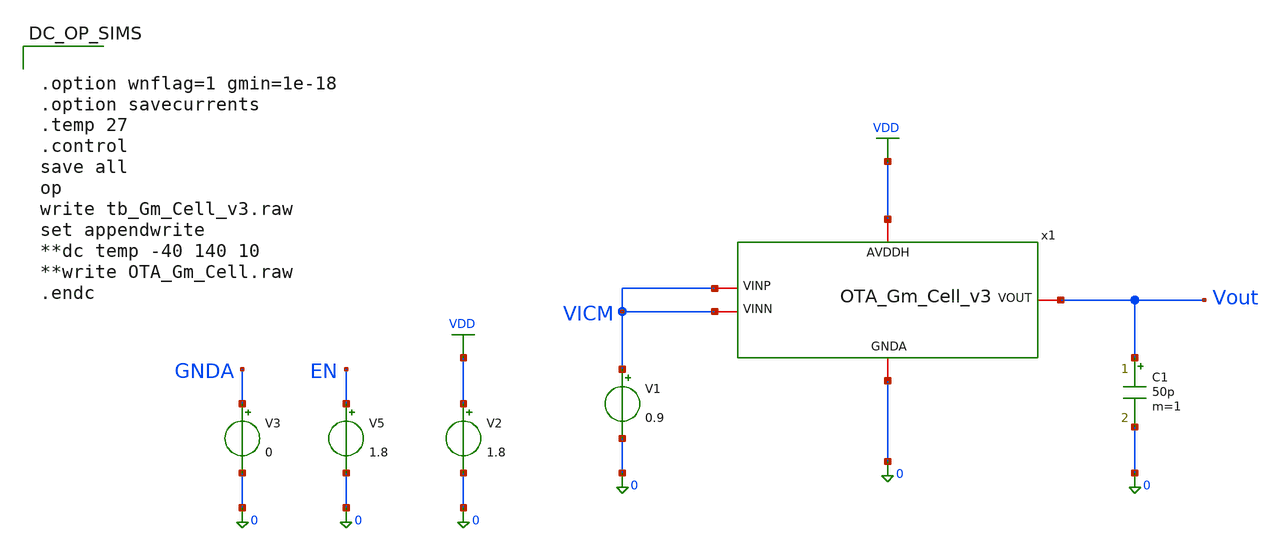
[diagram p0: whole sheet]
** sch_path: OTAs/NMOS_SrcDeg_SE_OTA_IntBias/SCH/tb_Gm_Cell_v3.sch
.lib $::SKYWATER_MODELS/sky130.lib.spice tt_mm
.include $::SKYWATER_STDCELLS/sky130_fd_sc_hd.spice

**.subckt tb_Gm_Cell_v3
x1 VDD VICM VICM Vout 0 OTA_Gm_Cell_v3
V1 VICM 0 0.9
V2 VDD 0 1.8
V3 GNDA 0 0
V5 EN 0 1.8
C1 Vout 0 50p m=1
**** begin user architecture code



.save @m.x1.xm1.msky130_fd_pr__nfet_01v8[gm]
.save @m.x1.xm1.msky130_fd_pr__nfet_01v8[gds]
.save @m.x1.xm1.msky130_fd_pr__nfet_01v8[vth]
.save @m.x1.xm1.msky130_fd_pr__nfet_01v8[vdsat]
.save @m.x1.xm1.msky130_fd_pr__nfet_01v8[cgg]
.save @m.x1.xm1.msky130_fd_pr__nfet_01v8[cgso]
.save @m.x1.xm1.msky130_fd_pr__nfet_01v8[cgdo]
.save @m.x1.xm3.msky130_fd_pr__pfet_01v8[gm]
.save @m.x1.xm3.msky130_fd_pr__pfet_01v8[gds]
.save @m.x1.xm3.msky130_fd_pr__pfet_01v8[vth]
.save @m.x1.xm3.msky130_fd_pr__pfet_01v8[vdsat]
.save @m.x1.xm3.msky130_fd_pr__pfet_01v8[cgg]
.save @m.x1.xm3.msky130_fd_pr__pfet_01v8[cgso]
.save @m.x1.xm3.msky130_fd_pr__pfet_01v8[cgdo]
.save @m.x1.xm4.msky130_fd_pr__pfet_01v8[gm]
.save @m.x1.xm4.msky130_fd_pr__pfet_01v8[gds]
.save @m.x1.xm4.msky130_fd_pr__pfet_01v8[vth]
.save @m.x1.xm4.msky130_fd_pr__pfet_01v8[vdsat]
.save @m.x1.xm4.msky130_fd_pr__pfet_01v8[cgg]
.save @m.x1.xm4.msky130_fd_pr__pfet_01v8[cgso]
.save @m.x1.xm4.msky130_fd_pr__pfet_01v8[cgdo]
.save @m.x1.xm5.msky130_fd_pr__pfet_01v8[gm]
.save @m.x1.xm5.msky130_fd_pr__pfet_01v8[gds]
.save @m.x1.xm5.msky130_fd_pr__pfet_01v8[vth]
.save @m.x1.xm5.msky130_fd_pr__pfet_01v8[vdsat]
.save @m.x1.xm5.msky130_fd_pr__pfet_01v8[cgg]
.save @m.x1.xm5.msky130_fd_pr__pfet_01v8[cgso]
.save @m.x1.xm5.msky130_fd_pr__pfet_01v8[cgdo]
.save @m.x1.xm6.msky130_fd_pr__pfet_01v8[gm]
.save @m.x1.xm6.msky130_fd_pr__pfet_01v8[gds]
.save @m.x1.xm6.msky130_fd_pr__pfet_01v8[vth]
.save @m.x1.xm6.msky130_fd_pr__pfet_01v8[vdsat]
.save @m.x1.xm6.msky130_fd_pr__pfet_01v8[cgg]
.save @m.x1.xm6.msky130_fd_pr__pfet_01v8[cgso]
.save @m.x1.xm6.msky130_fd_pr__pfet_01v8[cgdo]
.save @m.x1.xm7.msky130_fd_pr__nfet_01v8[gm]
.save @m.x1.xm7.msky130_fd_pr__nfet_01v8[gds]
.save @m.x1.xm7.msky130_fd_pr__nfet_01v8[vth]
.save @m.x1.xm7.msky130_fd_pr__nfet_01v8[vdsat]
.save @m.x1.xm7.msky130_fd_pr__nfet_01v8[cgg]
.save @m.x1.xm7.msky130_fd_pr__nfet_01v8[cgso]
.save @m.x1.xm7.msky130_fd_pr__nfet_01v8[cgdo]
.save @m.x1.xm10.msky130_fd_pr__nfet_01v8[gm]
.save @m.x1.xm10.msky130_fd_pr__nfet_01v8[gds]
.save @m.x1.xm10.msky130_fd_pr__nfet_01v8[vth]
.save @m.x1.xm10.msky130_fd_pr__nfet_01v8[vdsat]
.save @m.x1.xm10.msky130_fd_pr__nfet_01v8[cgg]
.save @m.x1.xm10.msky130_fd_pr__nfet_01v8[cgso]
.save @m.x1.xm10.msky130_fd_pr__nfet_01v8[cgdo]
.save @m.x1.xm12.msky130_fd_pr__pfet_01v8[gm]
.save @m.x1.xm12.msky130_fd_pr__pfet_01v8[gds]
.save @m.x1.xm12.msky130_fd_pr__pfet_01v8[vth]
.save @m.x1.xm12.msky130_fd_pr__pfet_01v8[vdsat]
.save @m.x1.xm12.msky130_fd_pr__pfet_01v8[cgg]
.save @m.x1.xm12.msky130_fd_pr__pfet_01v8[cgso]
.save @m.x1.xm12.msky130_fd_pr__pfet_01v8[cgdo]
.save @m.x1.xm15.msky130_fd_pr__pfet_01v8[gm]
.save @m.x1.xm15.msky130_fd_pr__pfet_01v8[gds]
.save @m.x1.xm15.msky130_fd_pr__pfet_01v8[vth]
.save @m.x1.xm15.msky130_fd_pr__pfet_01v8[vdsat]
.save @m.x1.xm15.msky130_fd_pr__pfet_01v8[cgg]
.save @m.x1.xm15.msky130_fd_pr__pfet_01v8[cgso]
.save @m.x1.xm15.msky130_fd_pr__pfet_01v8[cgdo]
.save @m.x1.xm16.msky130_fd_pr__nfet_01v8[gm]
.save @m.x1.xm16.msky130_fd_pr__nfet_01v8[gds]
.save @m.x1.xm16.msky130_fd_pr__nfet_01v8[vth]
.save @m.x1.xm16.msky130_fd_pr__nfet_01v8[vdsat]
.save @m.x1.xm16.msky130_fd_pr__nfet_01v8[cgg]
.save @m.x1.xm16.msky130_fd_pr__nfet_01v8[cgso]
.save @m.x1.xm16.msky130_fd_pr__nfet_01v8[cgdo]
.save @m.x1.xm8.msky130_fd_pr__pfet_01v8[gm]
.save @m.x1.xm8.msky130_fd_pr__pfet_01v8[gds]
.save @m.x1.xm8.msky130_fd_pr__pfet_01v8[vth]
.save @m.x1.xm8.msky130_fd_pr__pfet_01v8[vdsat]
.save @m.x1.xm8.msky130_fd_pr__pfet_01v8[cgg]
.save @m.x1.xm8.msky130_fd_pr__pfet_01v8[cgso]
.save @m.x1.xm8.msky130_fd_pr__pfet_01v8[cgdo]
.save @m.x1.xm9.msky130_fd_pr__pfet_01v8[gm]
.save @m.x1.xm9.msky130_fd_pr__pfet_01v8[gds]
.save @m.x1.xm9.msky130_fd_pr__pfet_01v8[vth]
.save @m.x1.xm9.msky130_fd_pr__pfet_01v8[vdsat]
.save @m.x1.xm9.msky130_fd_pr__pfet_01v8[cgg]
.save @m.x1.xm9.msky130_fd_pr__pfet_01v8[cgso]
.save @m.x1.xm9.msky130_fd_pr__pfet_01v8[cgdo]
.save @m.x1.xm2.msky130_fd_pr__pfet_01v8[gm]
.save @m.x1.xm2.msky130_fd_pr__pfet_01v8[gds]
.save @m.x1.xm2.msky130_fd_pr__pfet_01v8[vth]
.save @m.x1.xm2.msky130_fd_pr__pfet_01v8[vdsat]
.save @m.x1.xm2.msky130_fd_pr__pfet_01v8[cgg]
.save @m.x1.xm2.msky130_fd_pr__pfet_01v8[cgso]
.save @m.x1.xm2.msky130_fd_pr__pfet_01v8[cgdo]
.save @m.x1.xm11.msky130_fd_pr__pfet_01v8[gm]
.save @m.x1.xm11.msky130_fd_pr__pfet_01v8[gds]
.save @m.x1.xm11.msky130_fd_pr__pfet_01v8[vth]
.save @m.x1.xm11.msky130_fd_pr__pfet_01v8[vdsat]
.save @m.x1.xm11.msky130_fd_pr__pfet_01v8[cgg]
.save @m.x1.xm11.msky130_fd_pr__pfet_01v8[cgso]
.save @m.x1.xm11.msky130_fd_pr__pfet_01v8[cgdo]
.save @m.x1.xm19.msky130_fd_pr__nfet_01v8[gm]
.save @m.x1.xm19.msky130_fd_pr__nfet_01v8[gds]
.save @m.x1.xm19.msky130_fd_pr__nfet_01v8[vth]
.save @m.x1.xm19.msky130_fd_pr__nfet_01v8[vdsat]
.save @m.x1.xm19.msky130_fd_pr__nfet_01v8[cgg]
.save @m.x1.xm19.msky130_fd_pr__nfet_01v8[cgso]
.save @m.x1.xm19.msky130_fd_pr__nfet_01v8[cgdo]
.save @m.x1.xm20.msky130_fd_pr__nfet_01v8[gm]
.save @m.x1.xm20.msky130_fd_pr__nfet_01v8[gds]
.save @m.x1.xm20.msky130_fd_pr__nfet_01v8[vth]
.save @m.x1.xm20.msky130_fd_pr__nfet_01v8[vdsat]
.save @m.x1.xm20.msky130_fd_pr__nfet_01v8[cgg]
.save @m.x1.xm20.msky130_fd_pr__nfet_01v8[cgso]
.save @m.x1.xm20.msky130_fd_pr__nfet_01v8[cgdo]
.save @m.x1.xm21.msky130_fd_pr__nfet_01v8[gm]
.save @m.x1.xm21.msky130_fd_pr__nfet_01v8[gds]
.save @m.x1.xm21.msky130_fd_pr__nfet_01v8[vth]
.save @m.x1.xm21.msky130_fd_pr__nfet_01v8[vdsat]
.save @m.x1.xm21.msky130_fd_pr__nfet_01v8[cgg]
.save @m.x1.xm21.msky130_fd_pr__nfet_01v8[cgso]
.save @m.x1.xm21.msky130_fd_pr__nfet_01v8[cgdo]
.save @m.x1.xm26.msky130_fd_pr__nfet_01v8[gm]
.save @m.x1.xm26.msky130_fd_pr__nfet_01v8[gds]
.save @m.x1.xm26.msky130_fd_pr__nfet_01v8[vth]
.save @m.x1.xm26.msky130_fd_pr__nfet_01v8[vdsat]
.save @m.x1.xm26.msky130_fd_pr__nfet_01v8[cgg]
.save @m.x1.xm26.msky130_fd_pr__nfet_01v8[cgso]
.save @m.x1.xm26.msky130_fd_pr__nfet_01v8[cgdo]
.save @m.x1.xm27.msky130_fd_pr__nfet_01v8[gm]
.save @m.x1.xm27.msky130_fd_pr__nfet_01v8[gds]
.save @m.x1.xm27.msky130_fd_pr__nfet_01v8[vth]
.save @m.x1.xm27.msky130_fd_pr__nfet_01v8[vdsat]
.save @m.x1.xm27.msky130_fd_pr__nfet_01v8[cgg]
.save @m.x1.xm27.msky130_fd_pr__nfet_01v8[cgso]
.save @m.x1.xm27.msky130_fd_pr__nfet_01v8[cgdo]
.save @m.x1.xm28.msky130_fd_pr__nfet_01v8[gm]
.save @m.x1.xm28.msky130_fd_pr__nfet_01v8[gds]
.save @m.x1.xm28.msky130_fd_pr__nfet_01v8[vth]
.save @m.x1.xm28.msky130_fd_pr__nfet_01v8[vdsat]
.save @m.x1.xm28.msky130_fd_pr__nfet_01v8[cgg]
.save @m.x1.xm28.msky130_fd_pr__nfet_01v8[cgso]
.save @m.x1.xm28.msky130_fd_pr__nfet_01v8[cgdo]
.save @m.x1.xm29.msky130_fd_pr__nfet_01v8[gm]
.save @m.x1.xm29.msky130_fd_pr__nfet_01v8[gds]
.save @m.x1.xm29.msky130_fd_pr__nfet_01v8[vth]
.save @m.x1.xm29.msky130_fd_pr__nfet_01v8[vdsat]
.save @m.x1.xm29.msky130_fd_pr__nfet_01v8[cgg]
.save @m.x1.xm29.msky130_fd_pr__nfet_01v8[cgso]
.save @m.x1.xm29.msky130_fd_pr__nfet_01v8[cgdo]
.save @m.x1.xm30.msky130_fd_pr__nfet_01v8[gm]
.save @m.x1.xm30.msky130_fd_pr__nfet_01v8[gds]
.save @m.x1.xm30.msky130_fd_pr__nfet_01v8[vth]
.save @m.x1.xm30.msky130_fd_pr__nfet_01v8[vdsat]
.save @m.x1.xm30.msky130_fd_pr__nfet_01v8[cgg]
.save @m.x1.xm30.msky130_fd_pr__nfet_01v8[cgso]
.save @m.x1.xm30.msky130_fd_pr__nfet_01v8[cgdo]
.save @m.x1.xm31.msky130_fd_pr__nfet_01v8[gm]
.save @m.x1.xm31.msky130_fd_pr__nfet_01v8[gds]
.save @m.x1.xm31.msky130_fd_pr__nfet_01v8[vth]
.save @m.x1.xm31.msky130_fd_pr__nfet_01v8[vdsat]
.save @m.x1.xm31.msky130_fd_pr__nfet_01v8[cgg]
.save @m.x1.xm31.msky130_fd_pr__nfet_01v8[cgso]
.save @m.x1.xm31.msky130_fd_pr__nfet_01v8[cgdo]
.save @m.x1.xm32.msky130_fd_pr__nfet_01v8[gm]
.save @m.x1.xm32.msky130_fd_pr__nfet_01v8[gds]
.save @m.x1.xm32.msky130_fd_pr__nfet_01v8[vth]
.save @m.x1.xm32.msky130_fd_pr__nfet_01v8[vdsat]
.save @m.x1.xm32.msky130_fd_pr__nfet_01v8[cgg]
.save @m.x1.xm32.msky130_fd_pr__nfet_01v8[cgso]
.save @m.x1.xm32.msky130_fd_pr__nfet_01v8[cgdo]
.save @m.x1.xm33.msky130_fd_pr__nfet_01v8_lvt[gm]
.save @m.x1.xm33.msky130_fd_pr__nfet_01v8_lvt[gds]
.save @m.x1.xm33.msky130_fd_pr__nfet_01v8_lvt[vth]
.save @m.x1.xm33.msky130_fd_pr__nfet_01v8_lvt[vdsat]
.save @m.x1.xm33.msky130_fd_pr__nfet_01v8_lvt[cgg]
.save @m.x1.xm33.msky130_fd_pr__nfet_01v8_lvt[cgso]
.save @m.x1.xm33.msky130_fd_pr__nfet_01v8_lvt[cgdo]
.save @m.x1.xm34.msky130_fd_pr__nfet_01v8_lvt[gm]
.save @m.x1.xm34.msky130_fd_pr__nfet_01v8_lvt[gds]
.save @m.x1.xm34.msky130_fd_pr__nfet_01v8_lvt[vth]
.save @m.x1.xm34.msky130_fd_pr__nfet_01v8_lvt[vdsat]
.save @m.x1.xm34.msky130_fd_pr__nfet_01v8_lvt[cgg]
.save @m.x1.xm34.msky130_fd_pr__nfet_01v8_lvt[cgso]
.save @m.x1.xm34.msky130_fd_pr__nfet_01v8_lvt[cgdo]
.save @m.x1.xm35.msky130_fd_pr__nfet_01v8[gm]
.save @m.x1.xm35.msky130_fd_pr__nfet_01v8[gds]
.save @m.x1.xm35.msky130_fd_pr__nfet_01v8[vth]
.save @m.x1.xm35.msky130_fd_pr__nfet_01v8[vdsat]
.save @m.x1.xm35.msky130_fd_pr__nfet_01v8[cgg]
.save @m.x1.xm35.msky130_fd_pr__nfet_01v8[cgso]
.save @m.x1.xm35.msky130_fd_pr__nfet_01v8[cgdo]
.save @m.x1.xm36.msky130_fd_pr__nfet_01v8[gm]
.save @m.x1.xm36.msky130_fd_pr__nfet_01v8[gds]
.save @m.x1.xm36.msky130_fd_pr__nfet_01v8[vth]
.save @m.x1.xm36.msky130_fd_pr__nfet_01v8[vdsat]
.save @m.x1.xm36.msky130_fd_pr__nfet_01v8[cgg]
.save @m.x1.xm36.msky130_fd_pr__nfet_01v8[cgso]
.save @m.x1.xm36.msky130_fd_pr__nfet_01v8[cgdo]
.save @m.x1.xm37.msky130_fd_pr__pfet_01v8[gm]
.save @m.x1.xm37.msky130_fd_pr__pfet_01v8[gds]
.save @m.x1.xm37.msky130_fd_pr__pfet_01v8[vth]
.save @m.x1.xm37.msky130_fd_pr__pfet_01v8[vdsat]
.save @m.x1.xm37.msky130_fd_pr__pfet_01v8[cgg]
.save @m.x1.xm37.msky130_fd_pr__pfet_01v8[cgso]
.save @m.x1.xm37.msky130_fd_pr__pfet_01v8[cgdo]
.save @m.x1.xm38.msky130_fd_pr__nfet_01v8[gm]
.save @m.x1.xm38.msky130_fd_pr__nfet_01v8[gds]
.save @m.x1.xm38.msky130_fd_pr__nfet_01v8[vth]
.save @m.x1.xm38.msky130_fd_pr__nfet_01v8[vdsat]
.save @m.x1.xm38.msky130_fd_pr__nfet_01v8[cgg]
.save @m.x1.xm38.msky130_fd_pr__nfet_01v8[cgso]
.save @m.x1.xm38.msky130_fd_pr__nfet_01v8[cgdo]
.save @m.x1.xm39.msky130_fd_pr__nfet_01v8[gm]
.save @m.x1.xm39.msky130_fd_pr__nfet_01v8[gds]
.save @m.x1.xm39.msky130_fd_pr__nfet_01v8[vth]
.save @m.x1.xm39.msky130_fd_pr__nfet_01v8[vdsat]
.save @m.x1.xm39.msky130_fd_pr__nfet_01v8[cgg]
.save @m.x1.xm39.msky130_fd_pr__nfet_01v8[cgso]
.save @m.x1.xm39.msky130_fd_pr__nfet_01v8[cgdo]
.save @m.x1.xm40.msky130_fd_pr__pfet_01v8[gm]
.save @m.x1.xm40.msky130_fd_pr__pfet_01v8[gds]
.save @m.x1.xm40.msky130_fd_pr__pfet_01v8[vth]
.save @m.x1.xm40.msky130_fd_pr__pfet_01v8[vdsat]
.save @m.x1.xm40.msky130_fd_pr__pfet_01v8[cgg]
.save @m.x1.xm40.msky130_fd_pr__pfet_01v8[cgso]
.save @m.x1.xm40.msky130_fd_pr__pfet_01v8[cgdo]
.save @m.x1.xm41.msky130_fd_pr__pfet_01v8[gm]
.save @m.x1.xm41.msky130_fd_pr__pfet_01v8[gds]
.save @m.x1.xm41.msky130_fd_pr__pfet_01v8[vth]
.save @m.x1.xm41.msky130_fd_pr__pfet_01v8[vdsat]
.save @m.x1.xm41.msky130_fd_pr__pfet_01v8[cgg]
.save @m.x1.xm41.msky130_fd_pr__pfet_01v8[cgso]
.save @m.x1.xm41.msky130_fd_pr__pfet_01v8[cgdo]
.save @m.x1.xm42.msky130_fd_pr__nfet_01v8[gm]
.save @m.x1.xm42.msky130_fd_pr__nfet_01v8[gds]
.save @m.x1.xm42.msky130_fd_pr__nfet_01v8[vth]
.save @m.x1.xm42.msky130_fd_pr__nfet_01v8[vdsat]
.save @m.x1.xm42.msky130_fd_pr__nfet_01v8[cgg]
.save @m.x1.xm42.msky130_fd_pr__nfet_01v8[cgso]
.save @m.x1.xm42.msky130_fd_pr__nfet_01v8[cgdo]
.save @m.x1.xm43.msky130_fd_pr__pfet_01v8[gm]
.save @m.x1.xm43.msky130_fd_pr__pfet_01v8[gds]
.save @m.x1.xm43.msky130_fd_pr__pfet_01v8[vth]
.save @m.x1.xm43.msky130_fd_pr__pfet_01v8[vdsat]
.save @m.x1.xm43.msky130_fd_pr__pfet_01v8[cgg]
.save @m.x1.xm43.msky130_fd_pr__pfet_01v8[cgso]
.save @m.x1.xm43.msky130_fd_pr__pfet_01v8[cgdo]
.save @m.x1.xm44.msky130_fd_pr__pfet_01v8[gm]
.save @m.x1.xm44.msky130_fd_pr__pfet_01v8[gds]
.save @m.x1.xm44.msky130_fd_pr__pfet_01v8[vth]
.save @m.x1.xm44.msky130_fd_pr__pfet_01v8[vdsat]
.save @m.x1.xm44.msky130_fd_pr__pfet_01v8[cgg]
.save @m.x1.xm44.msky130_fd_pr__pfet_01v8[cgso]
.save @m.x1.xm44.msky130_fd_pr__pfet_01v8[cgdo]
.save @m.x1.xm45.msky130_fd_pr__nfet_01v8[gm]
.save @m.x1.xm45.msky130_fd_pr__nfet_01v8[gds]
.save @m.x1.xm45.msky130_fd_pr__nfet_01v8[vth]
.save @m.x1.xm45.msky130_fd_pr__nfet_01v8[vdsat]
.save @m.x1.xm45.msky130_fd_pr__nfet_01v8[cgg]
.save @m.x1.xm45.msky130_fd_pr__nfet_01v8[cgso]
.save @m.x1.xm45.msky130_fd_pr__nfet_01v8[cgdo]
.save @m.x1.xm46.msky130_fd_pr__pfet_01v8[gm]
.save @m.x1.xm46.msky130_fd_pr__pfet_01v8[gds]
.save @m.x1.xm46.msky130_fd_pr__pfet_01v8[vth]
.save @m.x1.xm46.msky130_fd_pr__pfet_01v8[vdsat]
.save @m.x1.xm46.msky130_fd_pr__pfet_01v8[cgg]
.save @m.x1.xm46.msky130_fd_pr__pfet_01v8[cgso]
.save @m.x1.xm46.msky130_fd_pr__pfet_01v8[cgdo]
.save @m.x1.xm47.msky130_fd_pr__pfet_01v8[gm]
.save @m.x1.xm47.msky130_fd_pr__pfet_01v8[gds]
.save @m.x1.xm47.msky130_fd_pr__pfet_01v8[vth]
.save @m.x1.xm47.msky130_fd_pr__pfet_01v8[vdsat]
.save @m.x1.xm47.msky130_fd_pr__pfet_01v8[cgg]
.save @m.x1.xm47.msky130_fd_pr__pfet_01v8[cgso]
.save @m.x1.xm47.msky130_fd_pr__pfet_01v8[cgdo]
.save @m.x1.xm48.msky130_fd_pr__pfet_01v8[gm]
.save @m.x1.xm48.msky130_fd_pr__pfet_01v8[gds]
.save @m.x1.xm48.msky130_fd_pr__pfet_01v8[vth]
.save @m.x1.xm48.msky130_fd_pr__pfet_01v8[vdsat]
.save @m.x1.xm48.msky130_fd_pr__pfet_01v8[cgg]
.save @m.x1.xm48.msky130_fd_pr__pfet_01v8[cgso]
.save @m.x1.xm48.msky130_fd_pr__pfet_01v8[cgdo]
.save @m.x1.xm49.msky130_fd_pr__pfet_01v8[gm]
.save @m.x1.xm49.msky130_fd_pr__pfet_01v8[gds]
.save @m.x1.xm49.msky130_fd_pr__pfet_01v8[vth]
.save @m.x1.xm49.msky130_fd_pr__pfet_01v8[vdsat]
.save @m.x1.xm49.msky130_fd_pr__pfet_01v8[cgg]
.save @m.x1.xm49.msky130_fd_pr__pfet_01v8[cgso]
.save @m.x1.xm49.msky130_fd_pr__pfet_01v8[cgdo]
.save @m.x1.xm50.msky130_fd_pr__pfet_01v8[gm]
.save @m.x1.xm50.msky130_fd_pr__pfet_01v8[gds]
.save @m.x1.xm50.msky130_fd_pr__pfet_01v8[vth]
.save @m.x1.xm50.msky130_fd_pr__pfet_01v8[vdsat]
.save @m.x1.xm50.msky130_fd_pr__pfet_01v8[cgg]
.save @m.x1.xm50.msky130_fd_pr__pfet_01v8[cgso]
.save @m.x1.xm50.msky130_fd_pr__pfet_01v8[cgdo]
.save @m.x1.xm51.msky130_fd_pr__pfet_01v8[gm]
.save @m.x1.xm51.msky130_fd_pr__pfet_01v8[gds]
.save @m.x1.xm51.msky130_fd_pr__pfet_01v8[vth]
.save @m.x1.xm51.msky130_fd_pr__pfet_01v8[vdsat]
.save @m.x1.xm51.msky130_fd_pr__pfet_01v8[cgg]
.save @m.x1.xm51.msky130_fd_pr__pfet_01v8[cgso]
.save @m.x1.xm51.msky130_fd_pr__pfet_01v8[cgdo]




.option wnflag=1 gmin=1e-18
.option savecurrents
.temp 27
.control
save all
op
write tb_Gm_Cell_v3.raw
set appendwrite
**dc temp -40 140 10
**write OTA_Gm_Cell.raw
.endc


**** end user architecture code
**.ends
.GLOBAL VDD
.end
